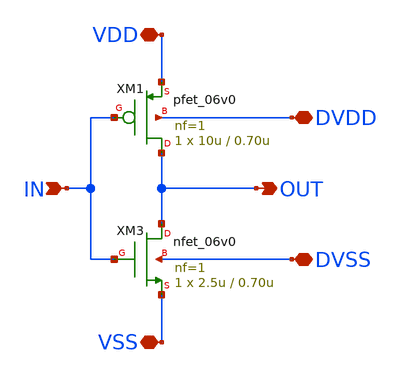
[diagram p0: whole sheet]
** sch_path: xschem/io_inv_2i.sch
* Copyright 2023 David Mitchell Bailey
* Licensed under the Apache License, Version 2.0 (the "License");
* you may not use this file except in compliance with the License.
* You may obtain a copy of the License at
* https://www.apache.org/licenses/LICENSE-2.0
* Unless required by applicable law or agreed to in writing, software
* distributed under the License is distributed on an "AS IS" BASIS,
* WITHOUT WARRANTIES OR CONDITIONS OF ANY KIND, either express or implied.
* See the License for the specific language governing permissions and
* limitations under the License.
**.subckt io_inv_2i OUT IN VDD VSS DVDD DVSS
*.opin OUT
*.ipin IN
*.iopin VDD
*.iopin VSS
*.iopin DVDD
*.iopin DVSS
XM1 OUT IN VDD DVDD pfet_06v0 L=0.70u W=10u nf=1 ad='int((nf+1)/2) * W/nf * 0.18u' as='int((nf+2)/2) * W/nf * 0.18u'
+ pd='2*int((nf+1)/2) * (W/nf + 0.18u)' ps='2*int((nf+2)/2) * (W/nf + 0.18u)' nrd='0.18u / W' nrs='0.18u / W'
+ sa=0 sb=0 sd=0 m=1
XM3 OUT IN VSS DVSS nfet_06v0 L=0.70u W=2.5u nf=1 ad='int((nf+1)/2) * W/nf * 0.18u' as='int((nf+2)/2) * W/nf * 0.18u'
+ pd='2*int((nf+1)/2) * (W/nf + 0.18u)' ps='2*int((nf+2)/2) * (W/nf + 0.18u)' nrd='0.18u / W' nrs='0.18u / W'
+ sa=0 sb=0 sd=0 m=1 par=1
**.ends
.end
